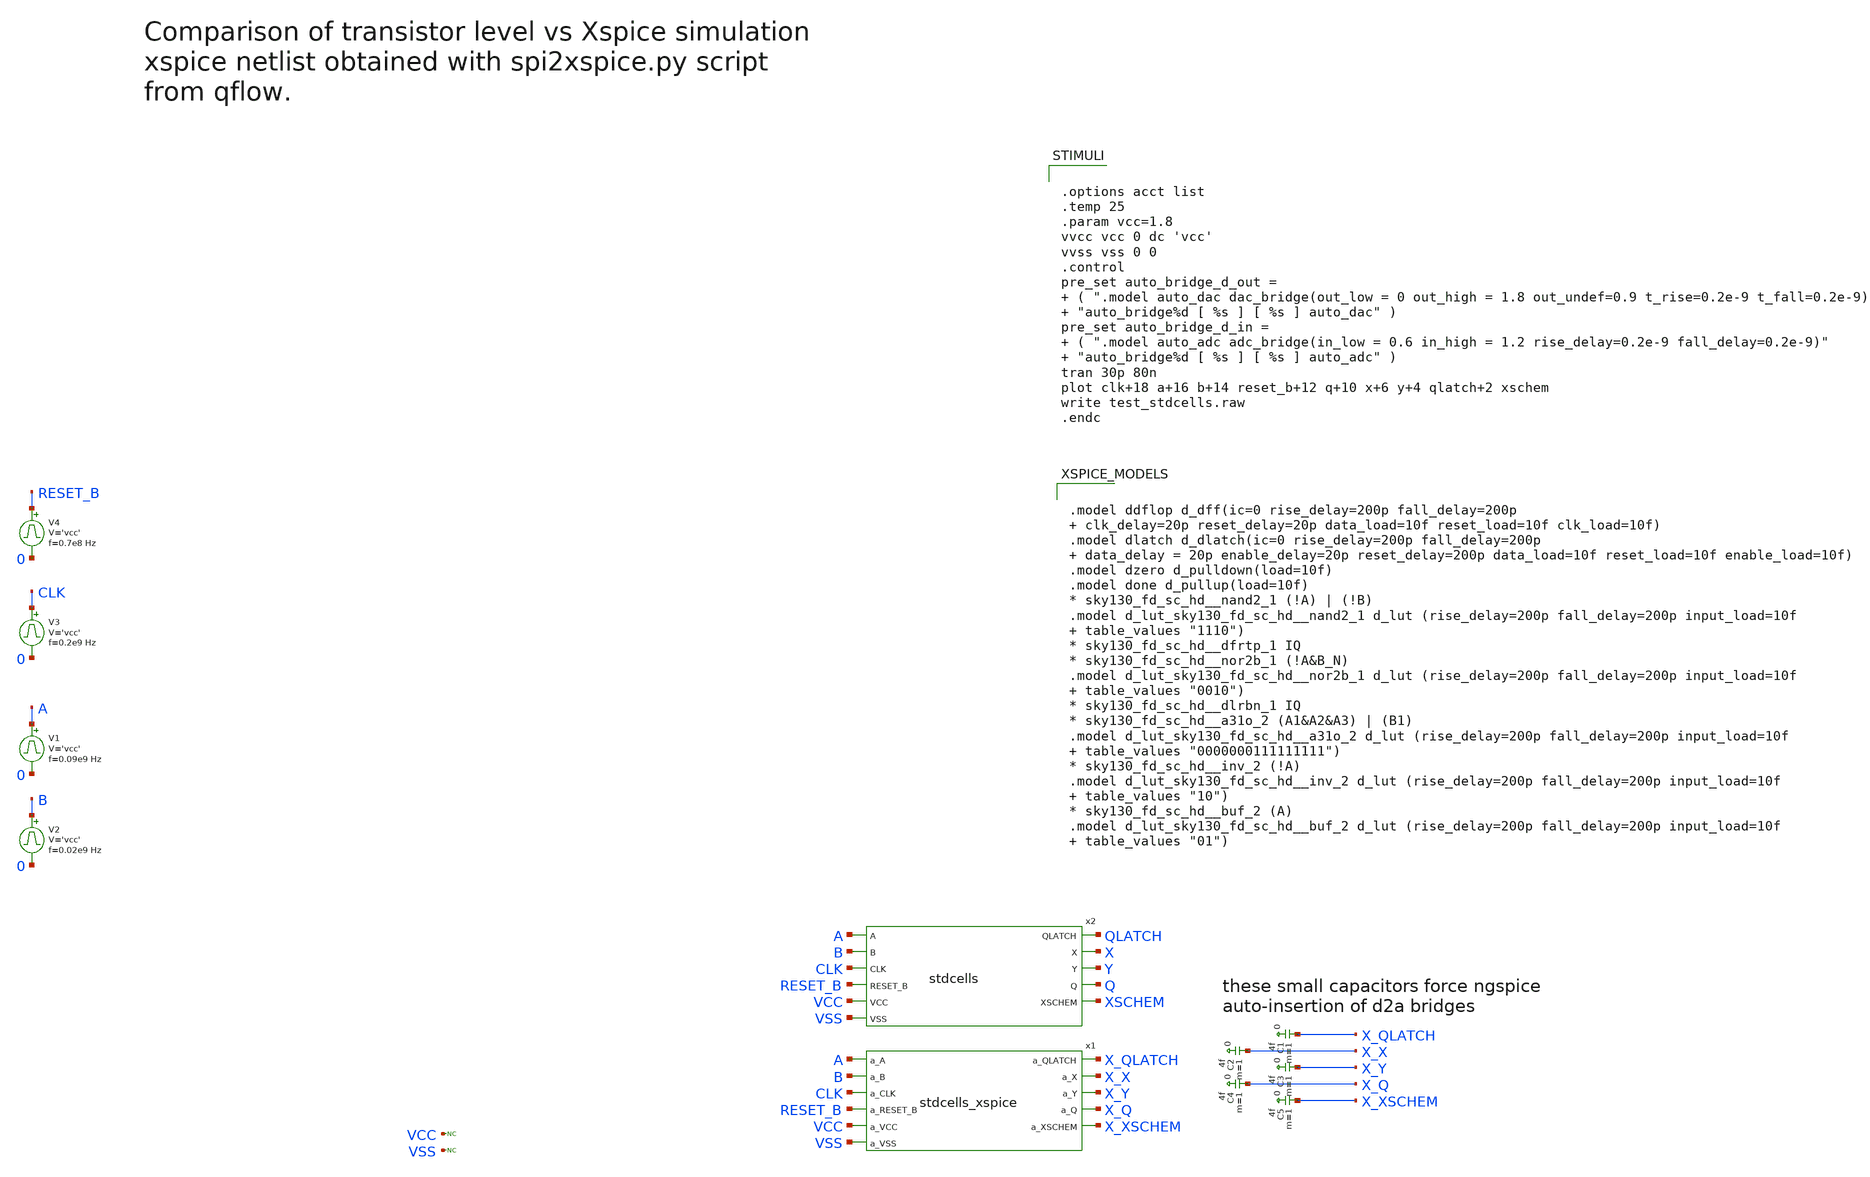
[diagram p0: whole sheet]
** sch_path: sky130A/xschem_libs/sky130_tests/test_stdcells/schematic/test_stdcells.sch
* Copyright 2021 Stefan Frederik Schippers
* Licensed under the Apache License, Version 2.0 (the "License");
* you may not use this file except in compliance with the License.
* You may obtain a copy of the License at
* https://www.apache.org/licenses/LICENSE-2.0
* Unless required by applicable law or agreed to in writing, software
* distributed under the License is distributed on an "AS IS" BASIS,
* WITHOUT WARRANTIES OR CONDITIONS OF ANY KIND, either express or implied.
* See the License for the specific language governing permissions and
* limitations under the License.
.lib $::SKYWATER_MODELS/sky130.lib.spice tt
.include $::SKYWATER_STDCELLS/sky130_fd_sc_hd.spice

**.subckt test_stdcells
V1 A 0 pulse 0 'vcc' '0.495/ 0.09e9 ' '0.01/0.09e9 ' '0.01/0.09e9 ' '0.49/0.09e9 ' '1/0.09e9 '
V2 B 0 pulse 0 'vcc' '0.495/ 0.02e9 ' '0.01/0.02e9 ' '0.01/0.02e9 ' '0.49/0.02e9 ' '1/0.02e9 '
V3 CLK 0 pulse 0 'vcc' '0.495/ 0.2e9 ' '0.01/0.2e9 ' '0.01/0.2e9 ' '0.49/0.2e9 ' '1/0.2e9 '
V4 RESET_B 0 pulse 0 'vcc' '0.495/ 0.7e8 ' '0.01/0.7e8 ' '0.01/0.7e8 ' '0.49/0.7e8 ' '1/0.7e8 '
x2 QLATCH A X B Y CLK Q RESET_B XSCHEM VCC VSS stdcells
x1 X_QLATCH A X_X B X_Y CLK X_Q RESET_B X_XSCHEM VCC VSS stdcells_xspice
* noconn VCC
* noconn VSS
C1 X_QLATCH 0 4f m=1
C2 X_X 0 4f m=1
C3 X_Y 0 4f m=1
C4 X_Q 0 4f m=1
C5 X_XSCHEM 0 4f m=1
**** begin user architecture code


.model ddflop d_dff(ic=0 rise_delay=200p fall_delay=200p  clk_delay=20p reset_delay=20p
+ data_load=10f reset_load=10f clk_load=10f)
.model dlatch d_dlatch(ic=0 rise_delay=200p fall_delay=200p  data_delay = 20p enable_delay=20p
+ reset_delay=200p data_load=10f reset_load=10f enable_load=10f)
.model dzero d_pulldown(load=10f)
.model done d_pullup(load=10f)
* sky130_fd_sc_hd__nand2_1 (!A) | (!B)
.model d_lut_sky130_fd_sc_hd__nand2_1 d_lut (rise_delay=200p fall_delay=200p input_load=10f
+  table_values "1110")
* sky130_fd_sc_hd__dfrtp_1 IQ
* sky130_fd_sc_hd__nor2b_1 (!A&B_N)
.model d_lut_sky130_fd_sc_hd__nor2b_1 d_lut (rise_delay=200p fall_delay=200p input_load=10f
+  table_values "0010")
* sky130_fd_sc_hd__dlrbn_1 IQ
* sky130_fd_sc_hd__a31o_2 (A1&A2&A3) | (B1)
.model d_lut_sky130_fd_sc_hd__a31o_2 d_lut (rise_delay=200p fall_delay=200p input_load=10f
+  table_values "0000000111111111")
* sky130_fd_sc_hd__inv_2 (!A)
.model d_lut_sky130_fd_sc_hd__inv_2 d_lut (rise_delay=200p fall_delay=200p input_load=10f
+  table_values "10")
* sky130_fd_sc_hd__buf_2 (A)
.model d_lut_sky130_fd_sc_hd__buf_2 d_lut (rise_delay=200p fall_delay=200p input_load=10f
+  table_values "01")




.options acct list
.temp 25
.param vcc=1.8
vvcc vcc 0 dc 'vcc'
vvss vss 0 0
.control
pre_set auto_bridge_d_out =  ( ".model auto_dac dac_bridge(out_low = 0 out_high = 1.8 out_undef=0.9
+ t_rise=0.2e-9 t_fall=0.2e-9)"  "auto_bridge%d [ %s ] [ %s ] auto_dac" )
pre_set auto_bridge_d_in =  ( ".model auto_adc adc_bridge(in_low = 0.6 in_high = 1.2
+ rise_delay=0.2e-9 fall_delay=0.2e-9)"  "auto_bridge%d [ %s ] [ %s ] auto_adc" )
tran 30p 80n
plot clk+18 a+16 b+14 reset_b+12 q+10 x+6 y+4 qlatch+2 xschem
write test_stdcells.raw
.endc


**** end user architecture code
**.ends

* expanding   symbol:  sky130_tests/stdcells.sym # of pins=11
** sym_path: sky130_tests/stdcells.sym
** sch_path: sky130_tests/stdcells.sch
.subckt stdcells QLATCH A X B Y CLK Q RESET_B XSCHEM VCC VSS
*.ipin RESET_B
*.ipin CLK
*.ipin B
*.ipin A
*.opin Y
*.opin X
*.opin QLATCH
*.opin Q
*.opin XSCHEM
*.ipin VCC
*.ipin VSS
x1 A B VSS VSS VCC VCC IX sky130_fd_sc_hd__nand2_1
C1 IX 0 3f m=1
x2 CLK A RESET_B VSS VSS VCC VCC IQ sky130_fd_sc_hd__dfrtp_1
C2 IQ 0 3f m=1
C3 IY 0 3f m=1
x3 A B VSS VSS VCC VCC IY sky130_fd_sc_hd__nor2b_1
x4 A CLK RESET_B VSS VSS VCC VCC IQLATCH net1 sky130_fd_sc_hd__dlrbn_1
C4 IQLATCH 0 3f m=1
x5 IY B VSS VSS VCC VCC net2 sky130_fd_sc_hd__nor2b_1
x6 net2 IQLATCH VSS VSS VCC VCC net4 sky130_fd_sc_hd__nand2_1
x7 net3 net4 IQ RESET_B VSS VSS VCC VCC IXSCHEM sky130_fd_sc_hd__a31o_2
* noconn #net1
* noconn IXSCHEM
x8 IY VSS VSS VCC VCC net3 sky130_fd_sc_hd__inv_2
x13 IY VSS VSS VCC VCC Y sky130_fd_sc_hd__buf_2
x9 IX VSS VSS VCC VCC X sky130_fd_sc_hd__buf_2
x14 IQ VSS VSS VCC VCC Q sky130_fd_sc_hd__buf_2
x15 IQLATCH VSS VSS VCC VCC QLATCH sky130_fd_sc_hd__buf_2
x11 IXSCHEM VSS VSS VCC VCC XSCHEM sky130_fd_sc_hd__buf_2
.ends


* expanding   symbol:  sky130_tests/stdcells_xspice.sym # of pins=11
** sym_path: sky130_tests/stdcells_xspice.sym
** sch_path: sky130_tests/stdcells_xspice.sch
.subckt stdcells_xspice a_QLATCH a_A a_X a_B a_Y a_CLK a_Q a_RESET_B a_XSCHEM a_VCC a_VSS
*.ipin a_RESET_B
*.ipin a_CLK
*.ipin a_B
*.ipin a_A
*.opin a_Y
*.opin a_X
*.opin a_QLATCH
*.opin a_Q
*.opin a_XSCHEM
*.ipin a_VCC
*.ipin a_VSS
**** begin user architecture code

A1 [A B] IX d_lut_sky130_fd_sc_hd__nand2_1
A2 A CLK NULL ~RESET_B IQ NULL ddflop
A3 [A B] IY d_lut_sky130_fd_sc_hd__nor2b_1
A4 A ~CLK NULL ~RESET_B IQLATCH NULL dlatch
A5 [IY B] net2 d_lut_sky130_fd_sc_hd__nor2b_1
A6 [net2 IQLATCH] net4 d_lut_sky130_fd_sc_hd__nand2_1
A7 [net3 net4 IQ RESET_B] IXSCHEM d_lut_sky130_fd_sc_hd__a31o_2
A8 [IY] net3 d_lut_sky130_fd_sc_hd__inv_2
A13 [IY] Y d_lut_sky130_fd_sc_hd__buf_2
A9 [IX] X d_lut_sky130_fd_sc_hd__buf_2
A14 [IQ] Q d_lut_sky130_fd_sc_hd__buf_2
A15 [IQLATCH] QLATCH d_lut_sky130_fd_sc_hd__buf_2
A11 [IXSCHEM] XSCHEM d_lut_sky130_fd_sc_hd__buf_2

AD2A1 [QLATCH] [a_QLATCH] toana_1v8
AA2D1 [a_A] [A] todig_1v8
AD2A2 [X] [a_X] toana_1v8
AA2D2 [a_B] [B] todig_1v8
AD2A3 [Y] [a_Y] toana_1v8
AA2D3 [a_CLK] [CLK] todig_1v8
AD2A4 [Q] [a_Q] toana_1v8
AA2D4 [a_RESET_B] [RESET_B] todig_1v8
AD2A5 [XSCHEM] [a_XSCHEM] toana_1v8
AA2D5 [a_VCC] [VCC] todig_1v8
AA2D6 [a_VSS] [VSS] todig_1v8


**** end user architecture code
.ends

.end
